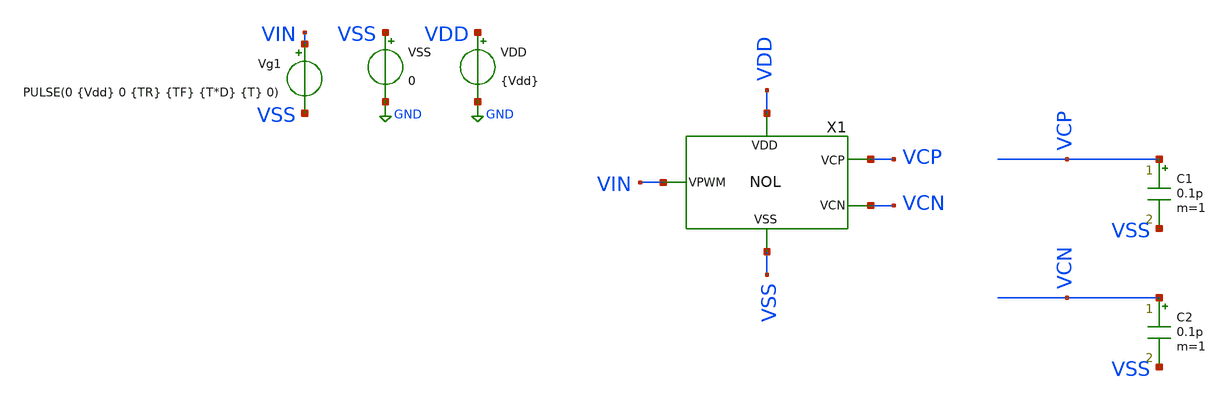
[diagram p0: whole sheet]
** sch_path: xschem/NOL/TB_NOL.sch
**.subckt TB_NOL
VDD VDD GND {Vdd}
VSS VSS GND 0
C1 VCP VSS 0.1p m=1
C2 VCN VSS 0.1p m=1
Vg1 VIN VSS PULSE(0 {Vdd} 0 {TR} {TF} {T*D} {T} 0)
X1 VCP VCN VIN VDD VSS NOL
**** begin user architecture code


.save all
.save v(vin) v(vcp) v(vcn)
.tran 10n {3*T}
.control
set color0 = white
run
plot v(vin) v(vcp)+2 v(vcn)+2
*plot v(vin) v(B2)+2 v(C2)+4 v(A1)+6 v(B1)+8 v(C1)+10 v(vcp)+12 v(vcn)+14
.endc

.measure tran tdead_fall  TRIG tran1.V(vcn) TD=0u VAL=0.9 FALL=1  TARG tran1.V(vcp) TD=0u VAL=0.9
+ FALL=1

.measure tran t_large_delay  TRIG tran1.V(x1.C1) TD=0u VAL=0.9 RISE=1  TARG tran1.V(x1.B2) TD=0u
+ VAL=0.9 RISE=1

.measure tran tdead_rise  TRIG tran1.V(vcp) TD=0u VAL=0.9 RISE=1  TARG tran1.V(vcn) TD=0u VAL=0.9
+ RISE=1






.param Vdd = 1.2
.param VH = 1.2
.param Del = 0

.param D = 0.4
.param fsw = 10Meg
.param T = 1/fsw
.csparam T = {T}
.param TR = 0.01*T
.param TF = 0.01*T
.param TdR = 0.01*T
.param TdF = 0.01*T


.param C_del = 0.1p
.param R_del_rise = TdR/(C_del)
.param R_del_fall = TdF/(C_del)

.param temp = 27





.param temp=27
.param mult = 1

.param w_P_NOR =0.15u
.param l_P_NOR = 0.15u

.param w_N_NOR =0.15u
.param l_N_NOR =0.15u

.param w_inv =0.15u
.param l_inv =0.15u






.lib cornerMOShv.lib mos_tt
.lib cornerMOSlv.lib mos_tt
*.lib cornerMOShv.lib mos_ff
*.lib cornerMOSlv.lib mos_ff
*.lib cornerMOShv.lib mos_ss
*.lib cornerMOSlv.lib mos_ss
*.lib cornerMOShv.lib mos_sf
*.lib cornerMOSlv.lib mos_sf
*.lib cornerMOShv.lib mos_fs
*.lib cornerMOSlv.lib mos_fs

*.include /opt/pdks/ihp-sg13g2/libs.ref/sg13g2_stdcell/spice/sg13g2_stdcell.spice
*.lib $::SG13G2_MODELS/cornerRES.lib res_typ
*.lib $::SG13G2_MODELS/cornerCAP.lib cap_typ
*.lib $::SG13G2_MODELS/diodes.lib

**** end user architecture code
**.ends

* expanding   symbol:  ../NOL/NOL.sym # of pins=5
** sym_path: xschem/NOL/NOL.sym
** sch_path: xschem/NOL/NOL.sch
.subckt NOL VCP VCN VPWM VDD VSS
*.iopin VDD
*.ipin VPWM
*.opin VCN
*.iopin VSS
*.opin VCP
C3 B2 VSS {C_del} m=1
R1 B1 C2 {R_del_fall} m=1
C4 B1 VSS {C_del} m=1
R2 B2 C1 {R_del_rise} m=1
X9 B2 net1 VDD VSS INV
X10 VDD VSS C1 A1 B1 NOR
X4 net1 VCN VDD VSS INV
X5 B1 net2 VDD VSS INV
X6 net2 net3 VDD VSS INV
X7 net3 VCP VDD VSS INV
X1 VPWM A1 VDD VSS INV
X2 VDD VSS C2 VPWM B2 NOR
**** begin user architecture code



**** end user architecture code
.ends


* expanding   symbol:  ../DigitalGates/INV.sym # of pins=4
** sym_path: xschem/DigitalGates/INV.sym
** sch_path: xschem/DigitalGates/INV.sch
.subckt INV X Y VDD VSS
*.iopin VDD
*.ipin X
*.opin Y
*.iopin VSS
XM3 Y X VSS VSS sg13_lv_nmos w={w_inv} l={l_inv} ng=1 m={mult} mm_ok=1
XM4 Y X VDD VDD sg13_lv_pmos w={w_inv} l={l_inv} ng=1 m={mult*3} mm_ok=1
**** begin user architecture code



**** end user architecture code
.ends


* expanding   symbol:  ../DigitalGates/NOR.sym # of pins=5
** sym_path: xschem/DigitalGates/NOR.sym
** sch_path: xschem/DigitalGates/NOR.sch
.subckt NOR VDD VSS F X Y
*.iopin VDD
*.ipin X
*.opin F
*.iopin VSS
*.ipin Y
XM1 F Y VSS VSS sg13_lv_nmos w={w_N_NOR} l={l_N_NOR} ng=1 m={mult} mm_ok=1
XM2 net1 X VDD VDD sg13_lv_pmos w={w_P_NOR} l={l_P_NOR} ng=1 m={mult*3} mm_ok=1
XM4 F Y net1 VDD sg13_lv_pmos w={w_P_NOR} l={l_P_NOR} ng=1 m={mult*3} mm_ok=1
XM3 F X VSS VSS sg13_lv_nmos w={w_N_NOR} l={l_N_NOR} ng=1 m={mult} mm_ok=1
**** begin user architecture code



**** end user architecture code
.ends

.GLOBAL GND
.end
